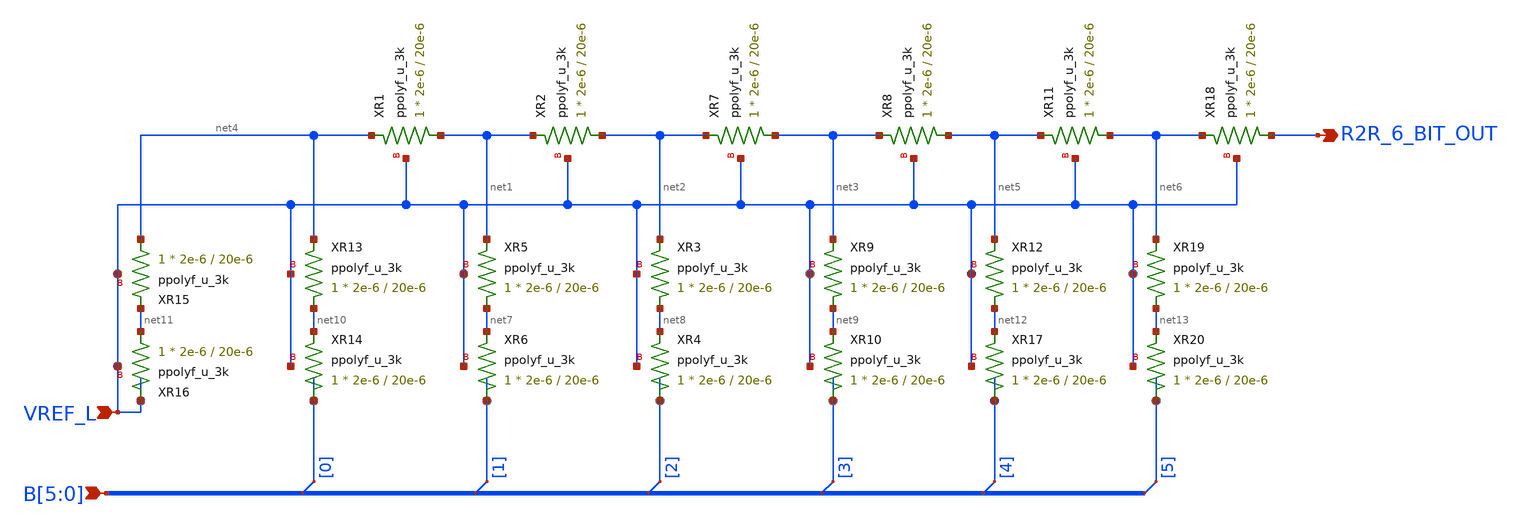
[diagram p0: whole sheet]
** sch_path: xschem/6_bit_r2r.sch
**.subckt 6_bit_r2r R2R_6_BIT_OUT VREF_L B[5],B[4],B[3],B[2],B[1],B[0]
*.opin R2R_6_BIT_OUT
*.ipin VREF_L
*.ipin B[5],B[4],B[3],B[2],B[1],B[0]
XR1 net1 net4 VREF_L ppolyf_u_3k r_width=2e-6 r_length=20e-6 m=1
XR2 net2 net1 VREF_L ppolyf_u_3k r_width=2e-6 r_length=20e-6 m=1
XR5 net7 net1 VREF_L ppolyf_u_3k r_width=2e-6 r_length=20e-6 m=1
XR6 B[1] net7 VREF_L ppolyf_u_3k r_width=2e-6 r_length=20e-6 m=1
XR3 net8 net2 VREF_L ppolyf_u_3k r_width=2e-6 r_length=20e-6 m=1
XR4 B[2] net8 VREF_L ppolyf_u_3k r_width=2e-6 r_length=20e-6 m=1
XR7 net3 net2 VREF_L ppolyf_u_3k r_width=2e-6 r_length=20e-6 m=1
XR8 net5 net3 VREF_L ppolyf_u_3k r_width=2e-6 r_length=20e-6 m=1
XR9 net9 net3 VREF_L ppolyf_u_3k r_width=2e-6 r_length=20e-6 m=1
XR10 B[3] net9 VREF_L ppolyf_u_3k r_width=2e-6 r_length=20e-6 m=1
XR13 net10 net4 VREF_L ppolyf_u_3k r_width=2e-6 r_length=20e-6 m=1
XR14 B[0] net10 VREF_L ppolyf_u_3k r_width=2e-6 r_length=20e-6 m=1
XR15 net4 net11 VREF_L ppolyf_u_3k r_width=2e-6 r_length=20e-6 m=1
XR16 net11 VREF_L VREF_L ppolyf_u_3k r_width=2e-6 r_length=20e-6 m=1
XR11 net6 net5 VREF_L ppolyf_u_3k r_width=2e-6 r_length=20e-6 m=1
XR12 net12 net5 VREF_L ppolyf_u_3k r_width=2e-6 r_length=20e-6 m=1
XR17 B[4] net12 VREF_L ppolyf_u_3k r_width=2e-6 r_length=20e-6 m=1
* tap: B[5:0] --> B[0]
* tap: B[5:0] --> B[1]
* tap: B[5:0] --> B[2]
* tap: B[5:0] --> B[3]
* tap: B[5:0] --> B[4]
XR18 R2R_6_BIT_OUT net6 VREF_L ppolyf_u_3k r_width=2e-6 r_length=20e-6 m=1
XR19 net13 net6 VREF_L ppolyf_u_3k r_width=2e-6 r_length=20e-6 m=1
XR20 B[5] net13 VREF_L ppolyf_u_3k r_width=2e-6 r_length=20e-6 m=1
* tap: B[5:0] --> B[5]
**.ends
.end
